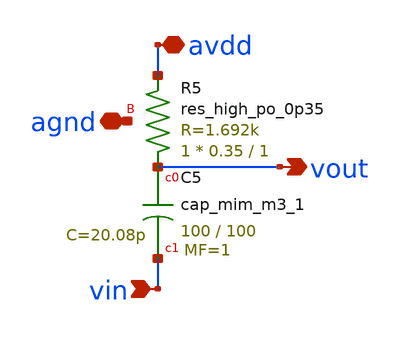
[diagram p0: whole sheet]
** sch_path: AMP/CPL_CM.sch
**.subckt CPL_CM vin vout agnd avdd
*.ipin vin
*.opin vout
*.iopin agnd
*.iopin avdd
XC5 vout vin sky130_fd_pr__cap_mim_m3_1 W=100 L=100 MF=1 m=1
XR5 vout avdd agnd sky130_fd_pr__res_high_po_0p35 L=1 mult=1 m=1
**.ends
.end
